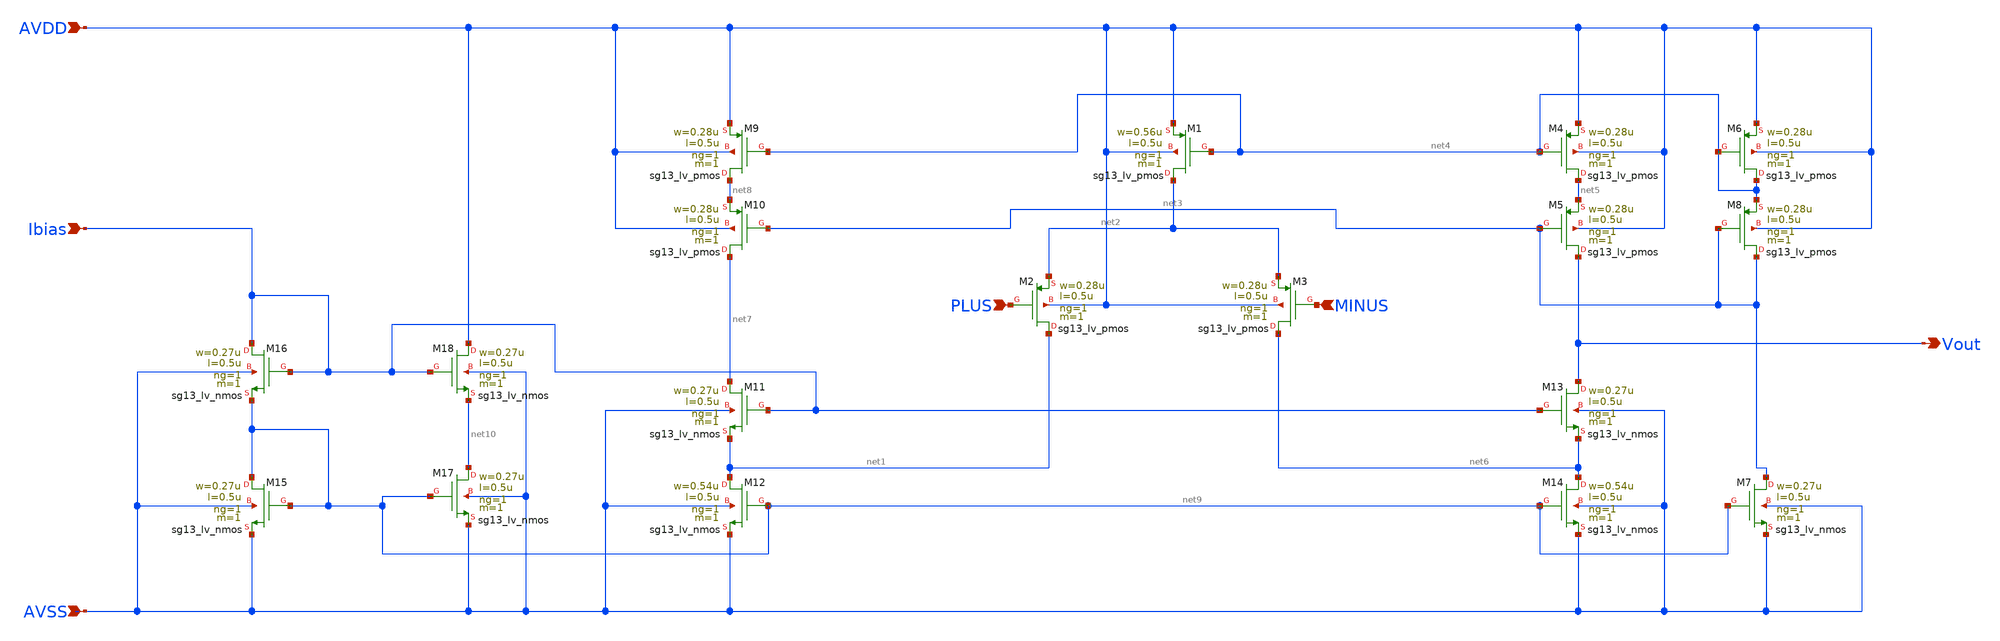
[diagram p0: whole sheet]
** sch_path: Designs/5t_ota/foldedcascode.sch
* (c) 2025 Thesis_HP, Apache-2.0 license
**.subckt foldedcascode PLUS MINUS Vout AVDD AVSS Ibias
*.ipin PLUS
*.ipin MINUS
*.opin Vout
*.ipin AVDD
*.ipin AVSS
*.ipin Ibias
XM1 net2 net4 AVDD AVDD sg13_lv_pmos w=0.56u l=0.5u ng=1 m=1 mm_ok=1
XM2 net1 PLUS net2 AVDD sg13_lv_pmos w=0.28u l=0.5u ng=1 m=1 mm_ok=1
XM3 net6 MINUS net2 AVDD sg13_lv_pmos w=0.28u l=0.5u ng=1 m=1 mm_ok=1
XM4 net5 net4 AVDD AVDD sg13_lv_pmos w=0.28u l=0.5u ng=1 m=1 mm_ok=1
XM5 Vout net3 net5 AVDD sg13_lv_pmos w=0.28u l=0.5u ng=1 m=1 mm_ok=1
XM14 net6 net9 AVSS AVSS sg13_lv_nmos w=0.54u l=0.5u ng=1 m=1 mm_ok=1
XM13 Vout Ibias net6 AVSS sg13_lv_nmos w=0.27u l=0.5u ng=1 m=1 mm_ok=1
XM11 net7 Ibias net1 AVSS sg13_lv_nmos w=0.27u l=0.5u ng=1 m=1 mm_ok=1
XM12 net1 net9 AVSS AVSS sg13_lv_nmos w=0.54u l=0.5u ng=1 m=1 mm_ok=1
XM7 net3 net9 AVSS AVSS sg13_lv_nmos w=0.27u l=0.5u ng=1 m=1 mm_ok=1
XM17 net10 net9 AVSS AVSS sg13_lv_nmos w=0.27u l=0.5u ng=1 m=1 mm_ok=1
XM18 AVDD Ibias net10 AVSS sg13_lv_nmos w=0.27u l=0.5u ng=1 m=1 mm_ok=1
XM8 net3 net3 net4 AVDD sg13_lv_pmos w=0.28u l=0.5u ng=1 m=1 mm_ok=1
XM6 net4 net4 AVDD AVDD sg13_lv_pmos w=0.28u l=0.5u ng=1 m=1 mm_ok=1
XM16 Ibias Ibias net9 AVSS sg13_lv_nmos w=0.27u l=0.5u ng=1 m=1 mm_ok=1
XM15 net9 net9 AVSS AVSS sg13_lv_nmos w=0.27u l=0.5u ng=1 m=1 mm_ok=1
XM10 net7 net3 net8 AVDD sg13_lv_pmos w=0.28u l=0.5u ng=1 m=1 mm_ok=1
XM9 net8 net4 AVDD AVDD sg13_lv_pmos w=0.28u l=0.5u ng=1 m=1 mm_ok=1
**.ends
.end
